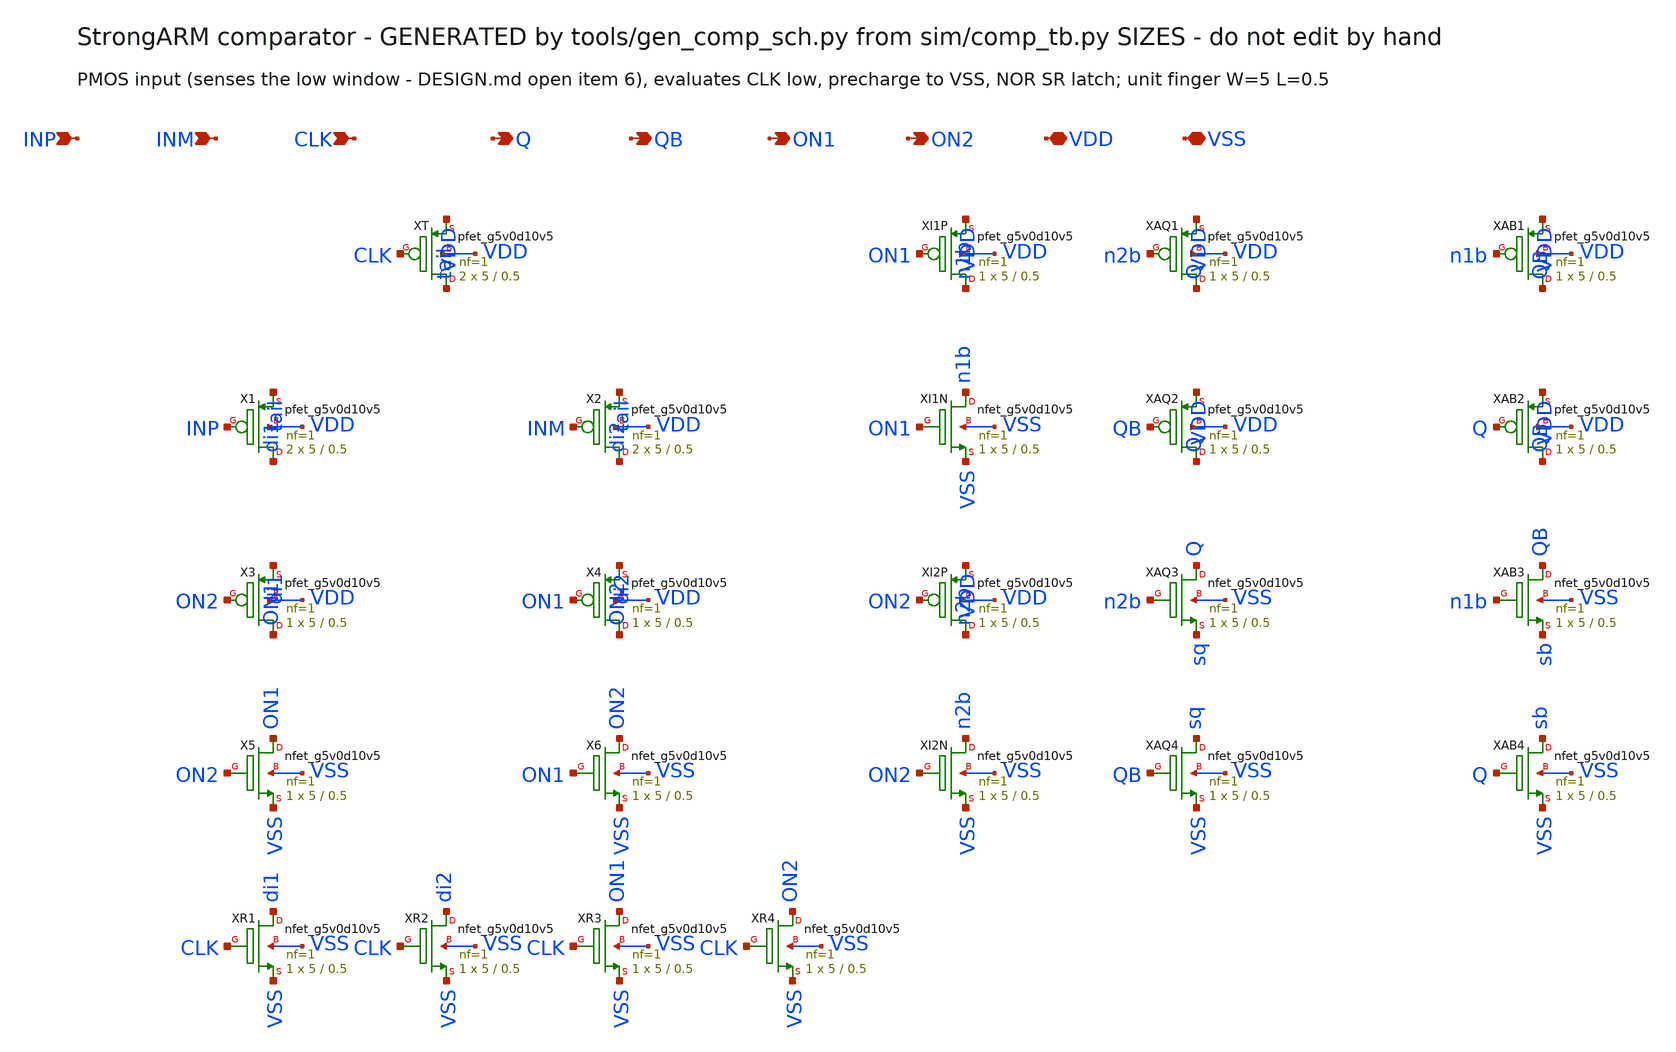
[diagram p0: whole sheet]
** sch_path: xschem/comp.sch
**.subckt comp INP INM CLK Q QB ON1 ON2 VDD VSS
*.ipin INP
*.ipin INM
*.ipin CLK
*.opin Q
*.opin QB
*.opin ON1
*.opin ON2
*.iopin VDD
*.iopin VSS
XXT tail CLK VDD VDD sky130_fd_pr__pfet_g5v0d10v5 L=0.5 W=5 nf=1 ad=0 as=0 pd=0 ps=0 nrd=0 nrs=0
+ sa=0 sb=0 sd=0 mult=2 m=2
XX1 di1 INP tail VDD sky130_fd_pr__pfet_g5v0d10v5 L=0.5 W=5 nf=1 ad=0 as=0 pd=0 ps=0 nrd=0 nrs=0
+ sa=0 sb=0 sd=0 mult=2 m=2
XX2 di2 INM tail VDD sky130_fd_pr__pfet_g5v0d10v5 L=0.5 W=5 nf=1 ad=0 as=0 pd=0 ps=0 nrd=0 nrs=0
+ sa=0 sb=0 sd=0 mult=2 m=2
XX3 ON1 ON2 di1 VDD sky130_fd_pr__pfet_g5v0d10v5 L=0.5 W=5 nf=1 ad=0 as=0 pd=0 ps=0 nrd=0 nrs=0 sa=0
+ sb=0 sd=0 mult=1 m=1
XX4 ON2 ON1 di2 VDD sky130_fd_pr__pfet_g5v0d10v5 L=0.5 W=5 nf=1 ad=0 as=0 pd=0 ps=0 nrd=0 nrs=0 sa=0
+ sb=0 sd=0 mult=1 m=1
XX5 ON1 ON2 VSS VSS sky130_fd_pr__nfet_g5v0d10v5 L=0.5 W=5 nf=1 ad=0 as=0 pd=0 ps=0 nrd=0 nrs=0 sa=0
+ sb=0 sd=0 mult=1 m=1
XX6 ON2 ON1 VSS VSS sky130_fd_pr__nfet_g5v0d10v5 L=0.5 W=5 nf=1 ad=0 as=0 pd=0 ps=0 nrd=0 nrs=0 sa=0
+ sb=0 sd=0 mult=1 m=1
XXR1 di1 CLK VSS VSS sky130_fd_pr__nfet_g5v0d10v5 L=0.5 W=5 nf=1 ad=0 as=0 pd=0 ps=0 nrd=0 nrs=0
+ sa=0 sb=0 sd=0 mult=1 m=1
XXR2 di2 CLK VSS VSS sky130_fd_pr__nfet_g5v0d10v5 L=0.5 W=5 nf=1 ad=0 as=0 pd=0 ps=0 nrd=0 nrs=0
+ sa=0 sb=0 sd=0 mult=1 m=1
XXR3 ON1 CLK VSS VSS sky130_fd_pr__nfet_g5v0d10v5 L=0.5 W=5 nf=1 ad=0 as=0 pd=0 ps=0 nrd=0 nrs=0
+ sa=0 sb=0 sd=0 mult=1 m=1
XXR4 ON2 CLK VSS VSS sky130_fd_pr__nfet_g5v0d10v5 L=0.5 W=5 nf=1 ad=0 as=0 pd=0 ps=0 nrd=0 nrs=0
+ sa=0 sb=0 sd=0 mult=1 m=1
XXI1P n1b ON1 VDD VDD sky130_fd_pr__pfet_g5v0d10v5 L=0.5 W=5 nf=1 ad=0 as=0 pd=0 ps=0 nrd=0 nrs=0
+ sa=0 sb=0 sd=0 mult=1 m=1
XXI1N n1b ON1 VSS VSS sky130_fd_pr__nfet_g5v0d10v5 L=0.5 W=5 nf=1 ad=0 as=0 pd=0 ps=0 nrd=0 nrs=0
+ sa=0 sb=0 sd=0 mult=1 m=1
XXI2P n2b ON2 VDD VDD sky130_fd_pr__pfet_g5v0d10v5 L=0.5 W=5 nf=1 ad=0 as=0 pd=0 ps=0 nrd=0 nrs=0
+ sa=0 sb=0 sd=0 mult=1 m=1
XXI2N n2b ON2 VSS VSS sky130_fd_pr__nfet_g5v0d10v5 L=0.5 W=5 nf=1 ad=0 as=0 pd=0 ps=0 nrd=0 nrs=0
+ sa=0 sb=0 sd=0 mult=1 m=1
XXAQ1 Q n2b VDD VDD sky130_fd_pr__pfet_g5v0d10v5 L=0.5 W=5 nf=1 ad=0 as=0 pd=0 ps=0 nrd=0 nrs=0 sa=0
+ sb=0 sd=0 mult=1 m=1
XXAQ2 Q QB VDD VDD sky130_fd_pr__pfet_g5v0d10v5 L=0.5 W=5 nf=1 ad=0 as=0 pd=0 ps=0 nrd=0 nrs=0 sa=0
+ sb=0 sd=0 mult=1 m=1
XXAQ3 Q n2b sq VSS sky130_fd_pr__nfet_g5v0d10v5 L=0.5 W=5 nf=1 ad=0 as=0 pd=0 ps=0 nrd=0 nrs=0 sa=0
+ sb=0 sd=0 mult=1 m=1
XXAQ4 sq QB VSS VSS sky130_fd_pr__nfet_g5v0d10v5 L=0.5 W=5 nf=1 ad=0 as=0 pd=0 ps=0 nrd=0 nrs=0 sa=0
+ sb=0 sd=0 mult=1 m=1
XXAB1 QB n1b VDD VDD sky130_fd_pr__pfet_g5v0d10v5 L=0.5 W=5 nf=1 ad=0 as=0 pd=0 ps=0 nrd=0 nrs=0
+ sa=0 sb=0 sd=0 mult=1 m=1
XXAB2 QB Q VDD VDD sky130_fd_pr__pfet_g5v0d10v5 L=0.5 W=5 nf=1 ad=0 as=0 pd=0 ps=0 nrd=0 nrs=0 sa=0
+ sb=0 sd=0 mult=1 m=1
XXAB3 QB n1b sb VSS sky130_fd_pr__nfet_g5v0d10v5 L=0.5 W=5 nf=1 ad=0 as=0 pd=0 ps=0 nrd=0 nrs=0 sa=0
+ sb=0 sd=0 mult=1 m=1
XXAB4 sb Q VSS VSS sky130_fd_pr__nfet_g5v0d10v5 L=0.5 W=5 nf=1 ad=0 as=0 pd=0 ps=0 nrd=0 nrs=0 sa=0
+ sb=0 sd=0 mult=1 m=1
**.ends
.end
